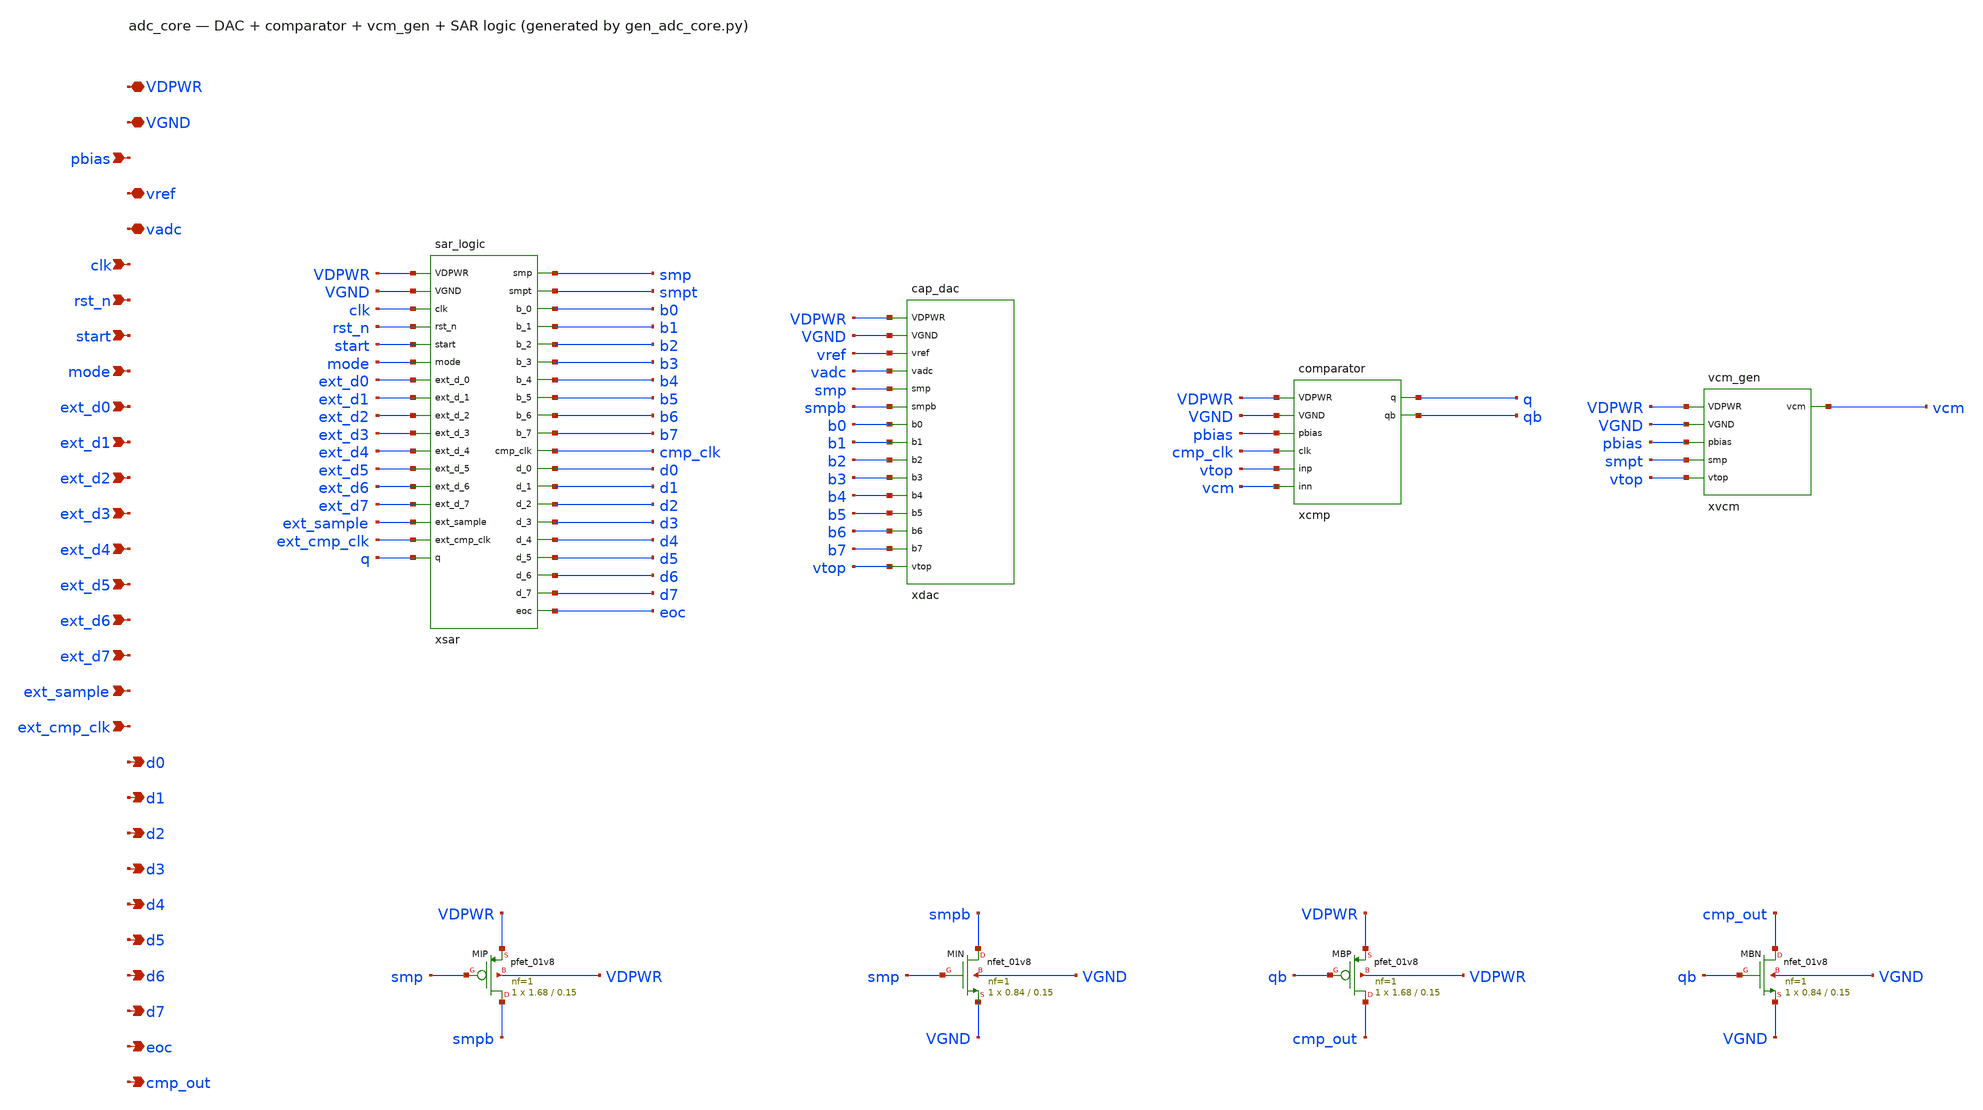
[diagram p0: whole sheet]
** sch_path: xschem/adc_core.sch
**.subckt adc_core VDPWR VGND pbias vref vadc clk rst_n start mode ext_d0 ext_d1 ext_d2 ext_d3
*+ ext_d4 ext_d5 ext_d6 ext_d7 ext_sample ext_cmp_clk d0 d1 d2 d3 d4 d5 d6 d7 eoc cmp_out
*.iopin VDPWR
*.iopin VGND
*.ipin pbias
*.iopin vref
*.iopin vadc
*.ipin clk
*.ipin rst_n
*.ipin start
*.ipin mode
*.ipin ext_d0
*.ipin ext_d1
*.ipin ext_d2
*.ipin ext_d3
*.ipin ext_d4
*.ipin ext_d5
*.ipin ext_d6
*.ipin ext_d7
*.ipin ext_sample
*.ipin ext_cmp_clk
*.opin d0
*.opin d1
*.opin d2
*.opin d3
*.opin d4
*.opin d5
*.opin d6
*.opin d7
*.opin eoc
*.opin cmp_out
xsar VDPWR VGND clk rst_n start mode ext_d0 ext_d1 ext_d2 ext_d3 ext_d4 ext_d5 ext_d6 ext_d7
+ ext_sample ext_cmp_clk q smp smpt b0 b1 b2 b3 b4 b5 b6 b7 cmp_clk d0 d1 d2 d3 d4 d5 d6 d7 eoc sar_logic
xdac VDPWR VGND vref vadc smp smpb b0 b1 b2 b3 b4 b5 b6 b7 vtop cap_dac
xcmp VDPWR VGND pbias cmp_clk vtop vcm q qb comparator
xvcm VDPWR VGND pbias smpt vtop vcm vcm_gen
XMIP smpb smp VDPWR VDPWR sky130_fd_pr__pfet_01v8 L=0.15 W=1.68 nf=1 ad='int((nf+1)/2) * W/nf * 0.29'
+ as='int((nf+2)/2) * W/nf * 0.29' pd='2*int((nf+1)/2) * (W/nf + 0.29)' ps='2*int((nf+2)/2) * (W/nf + 0.29)'
+ nrd='0.29 / W' nrs='0.29 / W' sa=0 sb=0 sd=0 mult=1 m=1
XMIN smpb smp VGND VGND sky130_fd_pr__nfet_01v8 L=0.15 W=0.84 nf=1 ad='int((1 + 1)/2) * 0.84 / 1 * 0.29'
+ as='int((1 + 2)/2) * 0.84 / 1 * 0.29' pd='2*int((1 + 1)/2) * (0.84 / 1 + 0.29)' ps='2*int((1 + 2)/2) * (0.84 / 1 + 0.29)'
+ nrd='0.29 / 0.84 ' nrs='0.29 / 0.84 ' sa=0 sb=0 sd=0 mult=1 m=1
XMBP cmp_out qb VDPWR VDPWR sky130_fd_pr__pfet_01v8 L=0.15 W=1.68 nf=1 ad='int((nf+1)/2) * W/nf * 0.29'
+ as='int((nf+2)/2) * W/nf * 0.29' pd='2*int((nf+1)/2) * (W/nf + 0.29)' ps='2*int((nf+2)/2) * (W/nf + 0.29)'
+ nrd='0.29 / W' nrs='0.29 / W' sa=0 sb=0 sd=0 mult=1 m=1
XMBN cmp_out qb VGND VGND sky130_fd_pr__nfet_01v8 L=0.15 W=0.84 nf=1 ad='int((1 + 1)/2) * 0.84 / 1 * 0.29'
+ as='int((1 + 2)/2) * 0.84 / 1 * 0.29' pd='2*int((1 + 1)/2) * (0.84 / 1 + 0.29)' ps='2*int((1 + 2)/2) * (0.84 / 1 + 0.29)'
+ nrd='0.29 / 0.84 ' nrs='0.29 / 0.84 ' sa=0 sb=0 sd=0 mult=1 m=1
**.ends
.end
